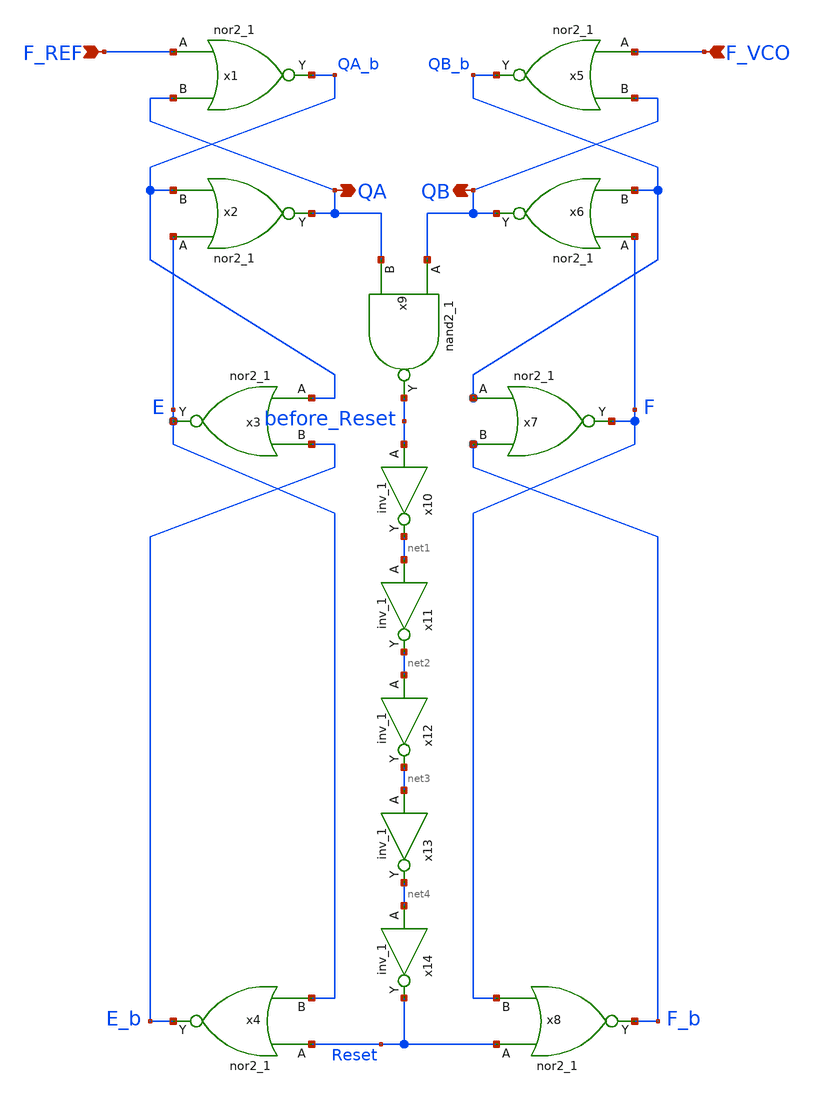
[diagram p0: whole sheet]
** sch_path: projects/pll/pfd/xschem_ngspice/phase_frequency_detector.sch
**.subckt phase_frequency_detector F_REF QA F_VCO QB
*.ipin F_REF
*.opin QA
*.ipin F_VCO
*.opin QB
x1 F_REF QA VGND VNB VPB VPWR QA_b sky130_fd_sc_hd__nor2_1
x2 E QA_b VGND VNB VPB VPWR QA sky130_fd_sc_hd__nor2_1
x3 QA_b E_b VGND VNB VPB VPWR E sky130_fd_sc_hd__nor2_1
x4 Reset E VGND VNB VPB VPWR E_b sky130_fd_sc_hd__nor2_1
x5 F_VCO QB VGND VNB VPB VPWR QB_b sky130_fd_sc_hd__nor2_1
x6 F QB_b VGND VNB VPB VPWR QB sky130_fd_sc_hd__nor2_1
x7 QB_b F_b VGND VNB VPB VPWR F sky130_fd_sc_hd__nor2_1
x8 Reset F VGND VNB VPB VPWR F_b sky130_fd_sc_hd__nor2_1
x9 QB QA VGND VNB VPB VPWR before_Reset sky130_fd_sc_hd__nand2_1
x10 before_Reset VGND VNB VPB VPWR net1 sky130_fd_sc_hd__inv_1
x11 net1 VGND VNB VPB VPWR net2 sky130_fd_sc_hd__inv_1
x12 net2 VGND VNB VPB VPWR net3 sky130_fd_sc_hd__inv_1
x13 net3 VGND VNB VPB VPWR net4 sky130_fd_sc_hd__inv_1
x14 net4 VGND VNB VPB VPWR Reset sky130_fd_sc_hd__inv_1
**.ends
.end
